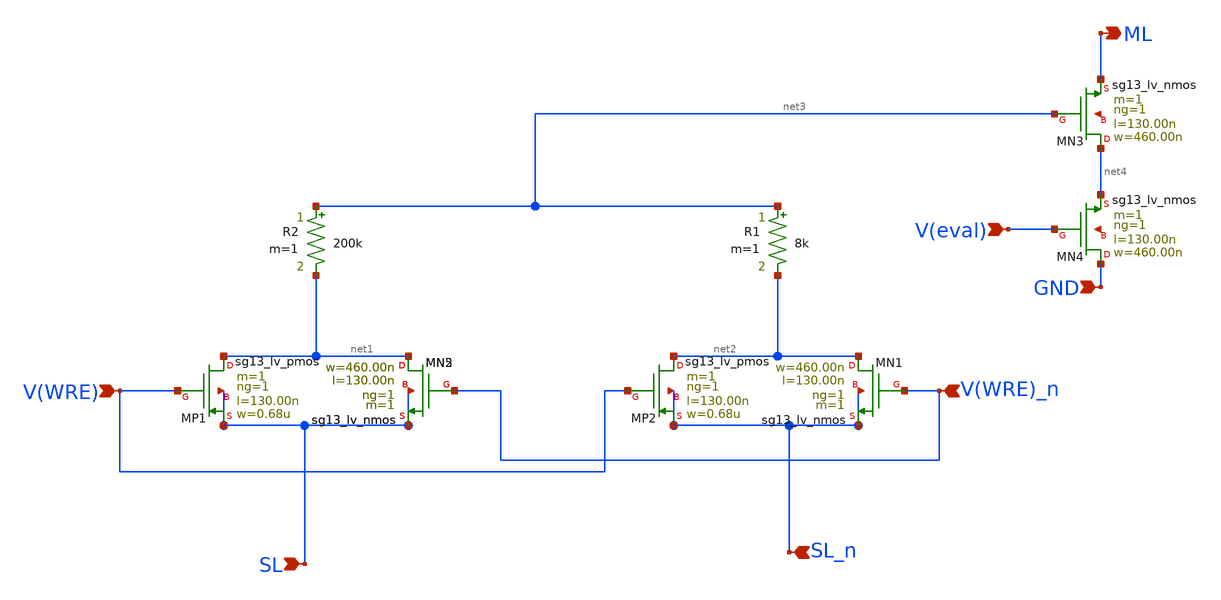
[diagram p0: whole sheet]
** sch_path: xschem/CELLMEM.sch
**.subckt CELLMEM V(WRE) V(WRE)_n SL SL_n V(eval) ML GND
*.ipin V(WRE)
*.ipin V(WRE)_n
*.ipin SL
*.ipin SL_n
*.ipin V(eval)
*.opin ML
*.ipin GND
XMP1 net1 V(WRE) SL SL sg13_lv_pmos w=0.68u l=130.00n ng=1 m=1 mm_ok=1
XMN5 net1 V(WRE)_n SL SL sg13_lv_nmos w=460.00n l=130.00n ng=1 m=1 mm_ok=1
XMP2 net2 V(WRE) SL_n SL_n sg13_lv_pmos w=0.68u l=130.00n ng=1 m=1 mm_ok=1
XMN1 net2 V(WRE)_n SL_n SL_n sg13_lv_nmos w=460.00n l=130.00n ng=1 m=1 mm_ok=1
R1 net3 net2 8k m=1
R2 net3 net1 200k m=1
XMN2 net1 V(WRE)_n SL SL sg13_lv_nmos w=460.00n l=130.00n ng=1 m=1 mm_ok=1
XMN3 net4 net3 ML net5 sg13_lv_nmos w=460.00n l=130.00n ng=1 m=1 mm_ok=1
XMN4 GND V(eval) net4 net6 sg13_lv_nmos w=460.00n l=130.00n ng=1 m=1 mm_ok=1
**.ends
.end
